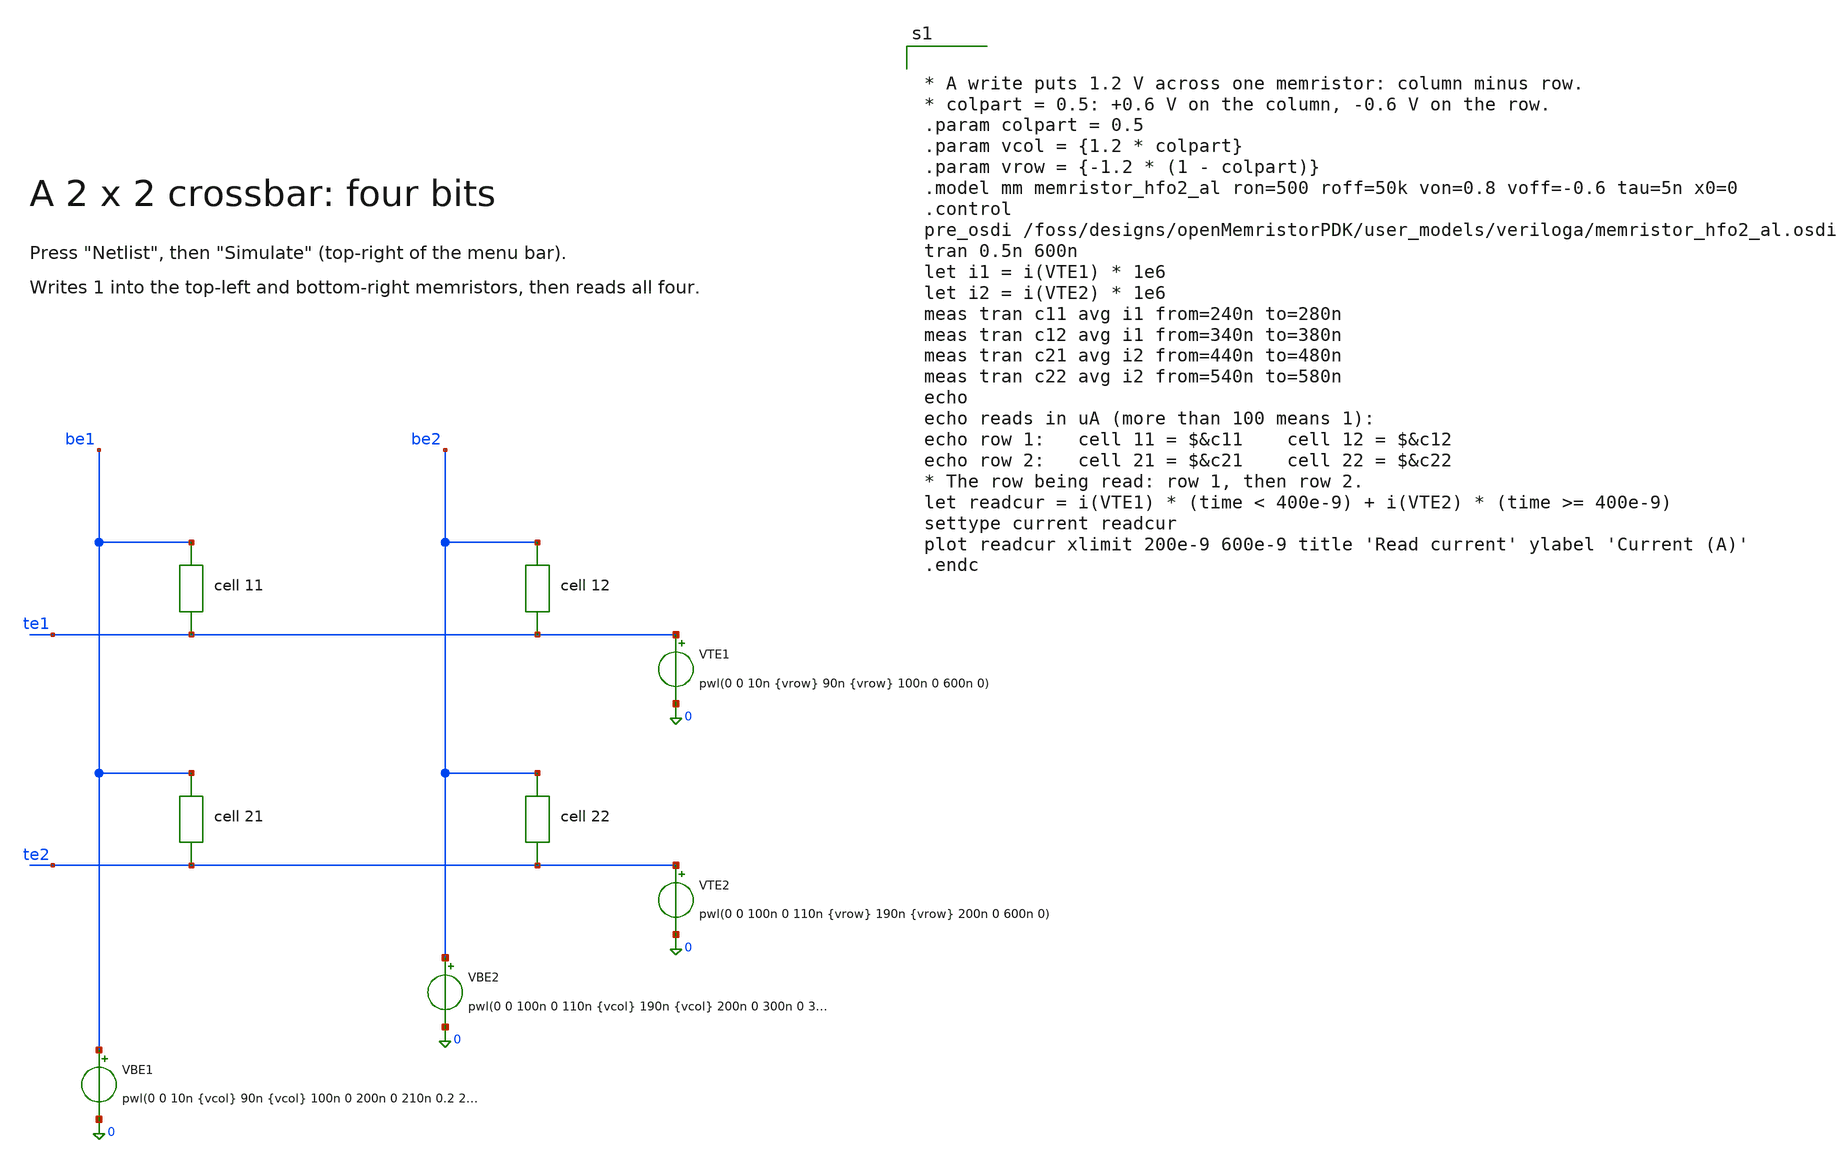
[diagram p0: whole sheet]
** sch_path: libraries/openmemristorpdk_pr/memristor_hfo2_al_crossbar2x2_tb.sch
**.subckt memristor_hfo2_al_crossbar2x2_tb
n11 be1 te1 mm
n12 be2 te1 mm
n21 be1 te2 mm
n22 be2 te2 mm
VBE1 be1 0 pwl(0 0 10n {vcol} 90n {vcol} 100n 0 200n 0 210n 0.2 290n 0.2 300n 0 400n 0 410n 0.2 490n
+ 0.2 500n 0 600n 0)
VBE2 be2 0 pwl(0 0 100n 0 110n {vcol} 190n {vcol} 200n 0 300n 0 310n 0.2 390n 0.2 400n 0 500n 0 510n
+ 0.2 590n 0.2 600n 0)
VTE1 te1 0 pwl(0 0 10n {vrow} 90n {vrow} 100n 0 600n 0)
VTE2 te2 0 pwl(0 0 100n 0 110n {vrow} 190n {vrow} 200n 0 600n 0)
**** begin user architecture code


* A write puts 1.2 V across one memristor: column minus row.
* colpart = 0.5: +0.6 V on the column, -0.6 V on the row.
.param colpart = 0.5
.param vcol = {1.2 * colpart}
.param vrow = {-1.2 * (1 - colpart)}
.model mm memristor_hfo2_al ron=500 roff=50k von=0.8 voff=-0.6 tau=5n x0=0
.control
pre_osdi /foss/designs/openMemristorPDK/user_models/veriloga/memristor_hfo2_al.osdi
tran 0.5n 600n
let i1 = i(VTE1) * 1e6
let i2 = i(VTE2) * 1e6
meas tran c11 avg i1 from=240n to=280n
meas tran c12 avg i1 from=340n to=380n
meas tran c21 avg i2 from=440n to=480n
meas tran c22 avg i2 from=540n to=580n
echo
echo reads in uA (more than 100 means 1):
echo row 1:   cell 11 = $&c11    cell 12 = $&c12
echo row 2:   cell 21 = $&c21    cell 22 = $&c22
* The row being read: row 1, then row 2.
let readcur = i(VTE1) * (time < 400e-9) + i(VTE2) * (time >= 400e-9)
settype current readcur
plot readcur xlimit 200e-9 600e-9 title 'Read current' ylabel 'Current (A)'
.endc


**** end user architecture code
**.ends
.end
